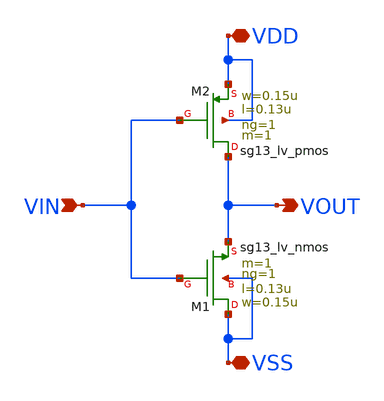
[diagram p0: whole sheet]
** sch_path: W2W-DAC/W2W_BOX/INV_D3.sch
**.subckt INV_D3 VDD VSS VOUT VIN
*.iopin VDD
*.iopin VSS
*.opin VOUT
*.ipin VIN
XM1 VSS VIN VOUT VSS sg13_lv_nmos w=0.15u l=0.13u ng=1 m=1 mm_ok=1
XM2 VOUT VIN VDD VDD sg13_lv_pmos w=0.15u l=0.13u ng=1 m=1 mm_ok=1
**.ends
.end
